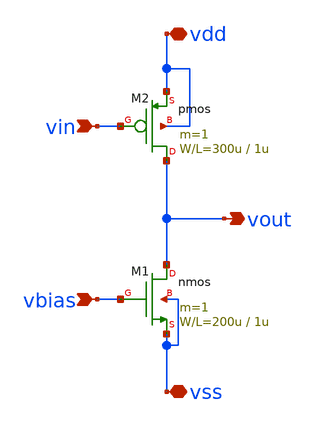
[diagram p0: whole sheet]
** sch_path: pfet_common_source_load_current.sch
**.subckt pfet_common_source_load_current vss vdd vin vout vbias
*.iopin vss
*.iopin vdd
*.ipin vin
*.opin vout
*.ipin vbias
M1 vout vbias vss vss nmos L=1u W=200u m=1
M2 vout vin vdd vdd pmos L=1u W=300u m=1
**** begin user architecture code
 .include $::LIB/mos.lib
.include $::LIB/passive.lib
.include $::LIB/diode.lib
**** end user architecture code
**.ends
.end
